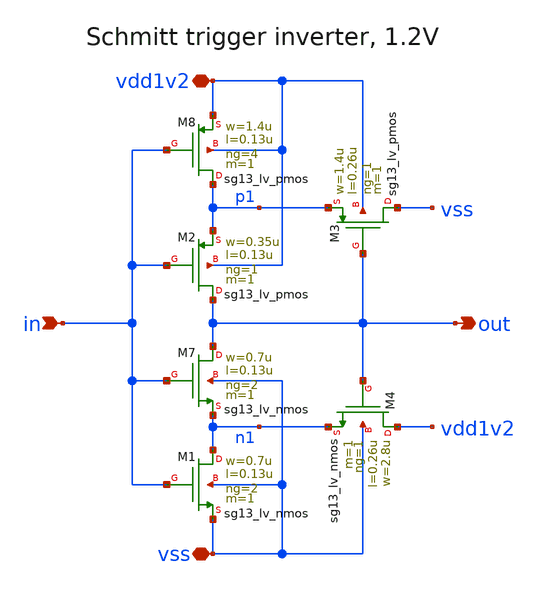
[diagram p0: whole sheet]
** sch_path: xschem/por_1v2_schmitt_inv.sch
**.subckt por_1v2_schmitt_inv vdd1v2 vss in out
*.iopin vdd1v2
*.iopin vss
*.ipin in
*.opin out
XM7 out in n1 vss sg13_lv_nmos w=0.7u l=0.13u ng=2 m=1 mm_ok=1
XM8 p1 in vdd1v2 vdd1v2 sg13_lv_pmos w=1.4u l=0.13u ng=4 m=1 mm_ok=1
XM2 out in p1 vdd1v2 sg13_lv_pmos w=0.35u l=0.13u ng=1 m=1 mm_ok=1
XM3 vss out p1 vdd1v2 sg13_lv_pmos w=1.4u l=0.26u ng=1 m=1 mm_ok=1
XM1 n1 in vss vss sg13_lv_nmos w=0.7u l=0.13u ng=2 m=1 mm_ok=1
XM4 vdd1v2 out n1 vss sg13_lv_nmos w=2.8u l=0.26u ng=1 m=1 mm_ok=1
**.ends
.end
